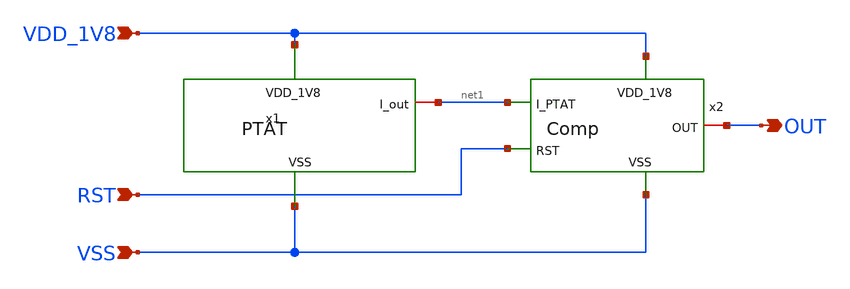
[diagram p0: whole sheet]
** sch_path: design/JNW_GR04_SKY130A/PTAT_TO_COMP.sch
**.subckt PTAT_TO_COMP VDD_1V8 VSS RST OUT
*.ipin VDD_1V8
*.ipin VSS
*.ipin RST
*.opin OUT
x1 VDD_1V8 net1 VSS PTAT
x2 VDD_1V8 OUT net1 RST VSS Comp
**.ends
.end
